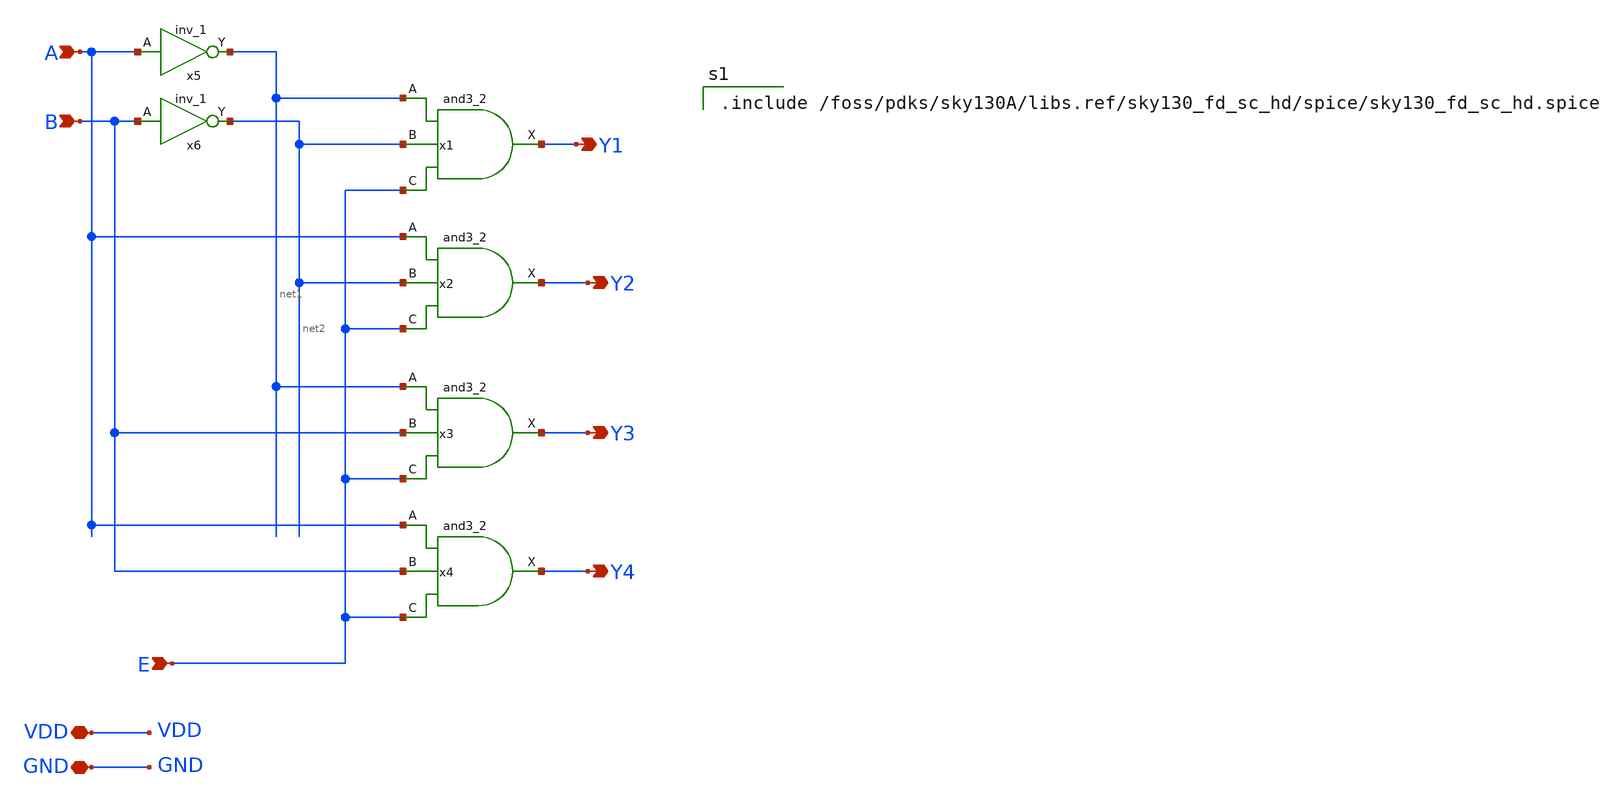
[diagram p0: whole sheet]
** sch_path: src/analog_source_files/2-4-decoder.sch
**.subckt 2-4-decoder E B A Y1 Y2 Y3 Y4 VDD GND
*.ipin E
*.ipin B
*.ipin A
*.opin Y1
*.opin Y2
*.opin Y3
*.opin Y4
*.iopin VDD
*.iopin GND
x1 net1 net2 E GND GND VDD VDD Y1 sky130_fd_sc_hd__and3_2
x2 A net2 E GND GND VDD VDD Y2 sky130_fd_sc_hd__and3_2
x3 net1 B E GND GND VDD VDD Y3 sky130_fd_sc_hd__and3_2
x4 A B E GND GND VDD VDD Y4 sky130_fd_sc_hd__and3_2
x5 A GND GND VDD VDD net1 sky130_fd_sc_hd__inv_1
x6 B GND GND VDD VDD net2 sky130_fd_sc_hd__inv_1
**** begin user architecture code

.include /foss/pdks/sky130A/libs.ref/sky130_fd_sc_hd/spice/sky130_fd_sc_hd.spice


**** end user architecture code
**.ends
.end
